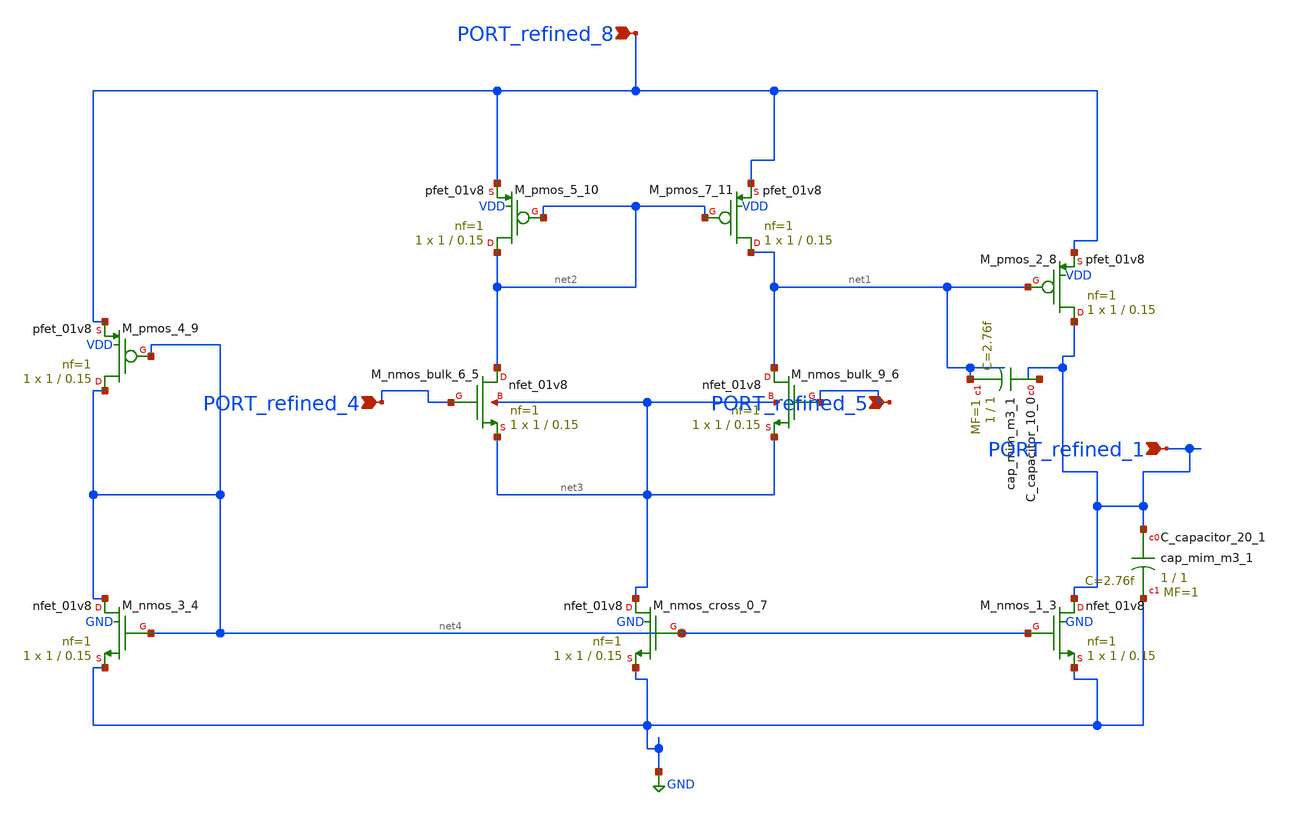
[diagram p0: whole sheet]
** sch_path: schematics/Image2Net/086.sch
**.subckt 086 PORT_refined_4 PORT_refined_5 PORT_refined_1 PORT_refined_8
*.ipin PORT_refined_4
*.ipin PORT_refined_5
*.ipin PORT_refined_1
*.ipin PORT_refined_8
XC_capacitor_10_0 PORT_refined_1 net1 sky130_fd_pr__cap_mim_m3_1 W=1 L=1 MF=1 m=1
XC_capacitor_20_1 PORT_refined_1 GND sky130_fd_pr__cap_mim_m3_1 W=1 L=1 MF=1 m=1
XM_nmos_1_3 PORT_refined_1 net4 GND GND sky130_fd_pr__nfet_01v8 L=0.15 W=1 nf=1 ad='int((1 + 1)/2) * 1 / 1 * 0.29'
+ as='int((1 + 2)/2) * 1 / 1 * 0.29' pd='2*int((1 + 1)/2) * (1 / 1 + 0.29)' ps='2*int((1 + 2)/2) * (1 / 1 + 0.29)'
+ nrd='0.29 / 1 ' nrs='0.29 / 1 ' sa=0 sb=0 sd=0 mult=1 m=1
XM_nmos_3_4 net4 net4 GND GND sky130_fd_pr__nfet_01v8 L=0.15 W=1 nf=1 ad='int((1 + 1)/2) * 1 / 1 * 0.29'
+ as='int((1 + 2)/2) * 1 / 1 * 0.29' pd='2*int((1 + 1)/2) * (1 / 1 + 0.29)' ps='2*int((1 + 2)/2) * (1 / 1 + 0.29)'
+ nrd='0.29 / 1 ' nrs='0.29 / 1 ' sa=0 sb=0 sd=0 mult=1 m=1
XM_nmos_bulk_6_5 net2 PORT_refined_4 net3 net3 sky130_fd_pr__nfet_01v8 L=0.15 W=1 nf=1 ad='int((1 + 1)/2) * 1 / 1 * 0.29'
+ as='int((1 + 2)/2) * 1 / 1 * 0.29' pd='2*int((1 + 1)/2) * (1 / 1 + 0.29)' ps='2*int((1 + 2)/2) * (1 / 1 + 0.29)'
+ nrd='0.29 / 1 ' nrs='0.29 / 1 ' sa=0 sb=0 sd=0 mult=1 m=1
XM_nmos_bulk_9_6 net1 PORT_refined_5 net3 net3 sky130_fd_pr__nfet_01v8 L=0.15 W=1 nf=1 ad='int((1 + 1)/2) * 1 / 1 * 0.29'
+ as='int((1 + 2)/2) * 1 / 1 * 0.29' pd='2*int((1 + 1)/2) * (1 / 1 + 0.29)' ps='2*int((1 + 2)/2) * (1 / 1 + 0.29)'
+ nrd='0.29 / 1 ' nrs='0.29 / 1 ' sa=0 sb=0 sd=0 mult=1 m=1
XM_nmos_cross_0_7 net3 net4 GND GND sky130_fd_pr__nfet_01v8 L=0.15 W=1 nf=1 ad='int((1 + 1)/2) * 1 / 1 * 0.29'
+ as='int((1 + 2)/2) * 1 / 1 * 0.29' pd='2*int((1 + 1)/2) * (1 / 1 + 0.29)' ps='2*int((1 + 2)/2) * (1 / 1 + 0.29)'
+ nrd='0.29 / 1 ' nrs='0.29 / 1 ' sa=0 sb=0 sd=0 mult=1 m=1
XM_pmos_2_8 PORT_refined_1 net1 PORT_refined_8 VDD sky130_fd_pr__pfet_01v8 L=0.15 W=1 nf=1 ad='int((1 + 1)/2) * 1 / 1 * 0.29'
+ as='int((1 + 2)/2) * 1 / 1 * 0.29' pd='2*int((1 + 1)/2) * (1 / 1 + 0.29)' ps='2*int((1 + 2)/2) * (1 / 1 + 0.29)'
+ nrd='0.29 / 1 ' nrs='0.29 / 1 ' sa=0 sb=0 sd=0 mult=1 m=1
XM_pmos_4_9 net4 net4 PORT_refined_8 VDD sky130_fd_pr__pfet_01v8 L=0.15 W=1 nf=1 ad='int((1 + 1)/2) * 1 / 1 * 0.29'
+ as='int((1 + 2)/2) * 1 / 1 * 0.29' pd='2*int((1 + 1)/2) * (1 / 1 + 0.29)' ps='2*int((1 + 2)/2) * (1 / 1 + 0.29)'
+ nrd='0.29 / 1 ' nrs='0.29 / 1 ' sa=0 sb=0 sd=0 mult=1 m=1
XM_pmos_5_10 net2 net2 PORT_refined_8 VDD sky130_fd_pr__pfet_01v8 L=0.15 W=1 nf=1 ad='int((1 + 1)/2) * 1 / 1 * 0.29'
+ as='int((1 + 2)/2) * 1 / 1 * 0.29' pd='2*int((1 + 1)/2) * (1 / 1 + 0.29)' ps='2*int((1 + 2)/2) * (1 / 1 + 0.29)'
+ nrd='0.29 / 1 ' nrs='0.29 / 1 ' sa=0 sb=0 sd=0 mult=1 m=1
XM_pmos_7_11 net1 net2 PORT_refined_8 VDD sky130_fd_pr__pfet_01v8 L=0.15 W=1 nf=1 ad='int((1 + 1)/2) * 1 / 1 * 0.29'
+ as='int((1 + 2)/2) * 1 / 1 * 0.29' pd='2*int((1 + 1)/2) * (1 / 1 + 0.29)' ps='2*int((1 + 2)/2) * (1 / 1 + 0.29)'
+ nrd='0.29 / 1 ' nrs='0.29 / 1 ' sa=0 sb=0 sd=0 mult=1 m=1
**.ends
.GLOBAL GND
.end
